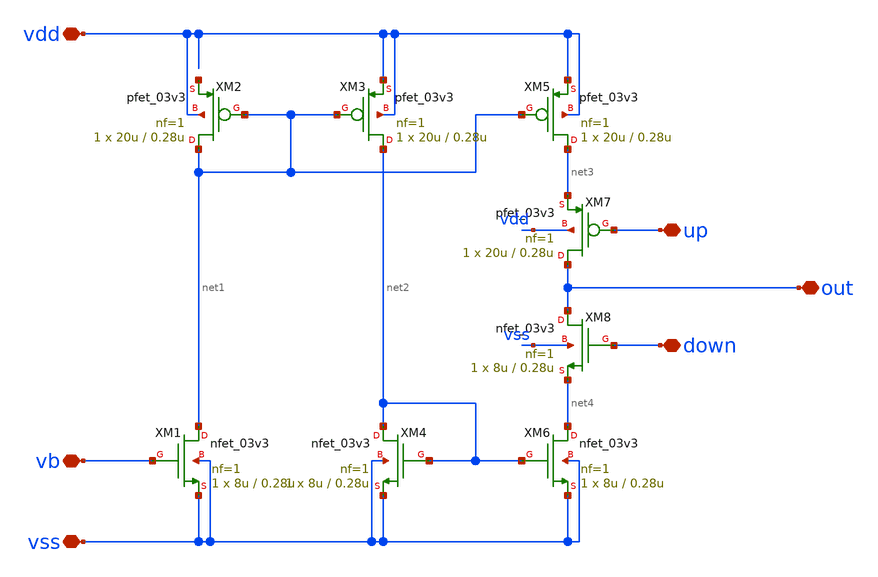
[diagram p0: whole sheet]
** sch_path: designs/libs/qw_core_analog_pkedit/chargepump.sch
**.subckt chargepump vdd vss vb up down out
*.iopin vdd
*.iopin vss
*.iopin vb
*.iopin up
*.iopin down
*.iopin out
XM1 net1 vb vss vss nfet_03v3 L=0.28u W=8u nf=1 ad='int((nf+1)/2) * W/nf * 0.18u' as='int((nf+2)/2) * W/nf * 0.18u'
+ pd='2*int((nf+1)/2) * (W/nf + 0.18u)' ps='2*int((nf+2)/2) * (W/nf + 0.18u)' nrd='0.18u / W' nrs='0.18u / W'
+ sa=0 sb=0 sd=0 m=1
XM2 net1 net1 net5 vdd pfet_03v3 L=0.28u W=20u nf=1 ad='int((nf+1)/2) * W/nf * 0.18u' as='int((nf+2)/2) * W/nf * 0.18u'
+ pd='2*int((nf+1)/2) * (W/nf + 0.18u)' ps='2*int((nf+2)/2) * (W/nf + 0.18u)' nrd='0.18u / W' nrs='0.18u / W'
+ sa=0 sb=0 sd=0 m=1
XM3 net2 net1 vdd vdd pfet_03v3 L=0.28u W=20u nf=1 ad='int((nf+1)/2) * W/nf * 0.18u' as='int((nf+2)/2) * W/nf * 0.18u'
+ pd='2*int((nf+1)/2) * (W/nf + 0.18u)' ps='2*int((nf+2)/2) * (W/nf + 0.18u)' nrd='0.18u / W' nrs='0.18u / W'
+ sa=0 sb=0 sd=0 m=1
XM4 net2 net2 vss vss nfet_03v3 L=0.28u W=8u nf=1 ad='int((nf+1)/2) * W/nf * 0.18u' as='int((nf+2)/2) * W/nf * 0.18u'
+ pd='2*int((nf+1)/2) * (W/nf + 0.18u)' ps='2*int((nf+2)/2) * (W/nf + 0.18u)' nrd='0.18u / W' nrs='0.18u / W'
+ sa=0 sb=0 sd=0 m=1
XM5 net3 net1 vdd vdd pfet_03v3 L=0.28u W=20u nf=1 ad='int((nf+1)/2) * W/nf * 0.18u' as='int((nf+2)/2) * W/nf * 0.18u'
+ pd='2*int((nf+1)/2) * (W/nf + 0.18u)' ps='2*int((nf+2)/2) * (W/nf + 0.18u)' nrd='0.18u / W' nrs='0.18u / W'
+ sa=0 sb=0 sd=0 m=1
XM6 net4 net2 vss vss nfet_03v3 L=0.28u W=8u nf=1 ad='int((nf+1)/2) * W/nf * 0.18u' as='int((nf+2)/2) * W/nf * 0.18u'
+ pd='2*int((nf+1)/2) * (W/nf + 0.18u)' ps='2*int((nf+2)/2) * (W/nf + 0.18u)' nrd='0.18u / W' nrs='0.18u / W'
+ sa=0 sb=0 sd=0 m=1
XM7 out up net3 vdd pfet_03v3 L=0.28u W=20u nf=1 ad='int((nf+1)/2) * W/nf * 0.18u' as='int((nf+2)/2) * W/nf * 0.18u'
+ pd='2*int((nf+1)/2) * (W/nf + 0.18u)' ps='2*int((nf+2)/2) * (W/nf + 0.18u)' nrd='0.18u / W' nrs='0.18u / W'
+ sa=0 sb=0 sd=0 m=1
XM8 out down net4 vss nfet_03v3 L=0.28u W=8u nf=1 ad='int((nf+1)/2) * W/nf * 0.18u' as='int((nf+2)/2) * W/nf * 0.18u'
+ pd='2*int((nf+1)/2) * (W/nf + 0.18u)' ps='2*int((nf+2)/2) * (W/nf + 0.18u)' nrd='0.18u / W' nrs='0.18u / W'
+ sa=0 sb=0 sd=0 m=1
**.ends
.end
